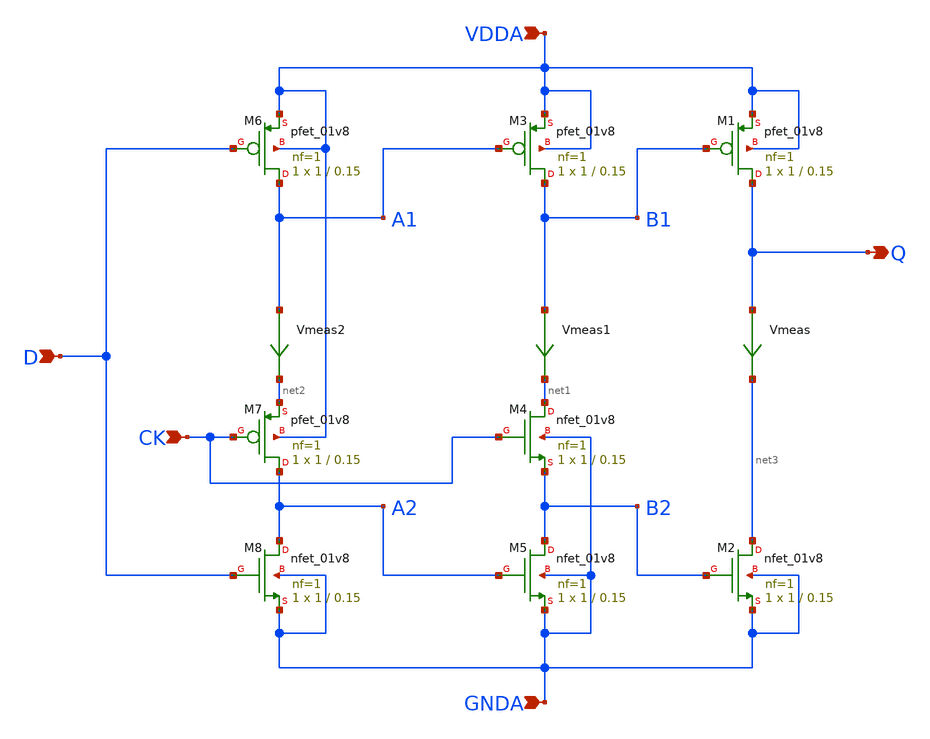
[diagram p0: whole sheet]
** sch_path: projects/pll/divider/xschem_ngspice/TSPC_FF_split_path.sch
**.subckt TSPC_FF_split_path CK D Q VDDA GNDA
*.ipin CK
*.ipin D
*.opin Q
*.ipin VDDA
*.ipin GNDA
XM1 Q B1 VDDA VDDA sky130_fd_pr__pfet_01v8 L=0.15 W=1 nf=1 ad='int((nf+1)/2) * W/nf * 0.29' as='int((nf+2)/2) * W/nf * 0.29'
+ pd='2*int((nf+1)/2) * (W/nf + 0.29)' ps='2*int((nf+2)/2) * (W/nf + 0.29)' nrd='0.29 / W' nrs='0.29 / W'
+ sa=0 sb=0 sd=0 mult=1 m=1
XM4 net1 CK B2 GNDA sky130_fd_pr__nfet_01v8 L=0.15 W=1 nf=1 ad='int((nf+1)/2) * W/nf * 0.29' as='int((nf+2)/2) * W/nf * 0.29'
+ pd='2*int((nf+1)/2) * (W/nf + 0.29)' ps='2*int((nf+2)/2) * (W/nf + 0.29)' nrd='0.29 / W' nrs='0.29 / W'
+ sa=0 sb=0 sd=0 mult=1 m=1
Vmeas Q net3 0
.save i(vmeas)
XM2 net3 B2 GNDA GNDA sky130_fd_pr__nfet_01v8 L=0.15 W=1 nf=1 ad='int((nf+1)/2) * W/nf * 0.29' as='int((nf+2)/2) * W/nf * 0.29'
+ pd='2*int((nf+1)/2) * (W/nf + 0.29)' ps='2*int((nf+2)/2) * (W/nf + 0.29)' nrd='0.29 / W' nrs='0.29 / W'
+ sa=0 sb=0 sd=0 mult=1 m=1
XM3 B1 A1 VDDA VDDA sky130_fd_pr__pfet_01v8 L=0.15 W=1 nf=1 ad='int((nf+1)/2) * W/nf * 0.29' as='int((nf+2)/2) * W/nf * 0.29'
+ pd='2*int((nf+1)/2) * (W/nf + 0.29)' ps='2*int((nf+2)/2) * (W/nf + 0.29)' nrd='0.29 / W' nrs='0.29 / W'
+ sa=0 sb=0 sd=0 mult=1 m=1
XM5 B2 A2 GNDA GNDA sky130_fd_pr__nfet_01v8 L=0.15 W=1 nf=1 ad='int((nf+1)/2) * W/nf * 0.29' as='int((nf+2)/2) * W/nf * 0.29'
+ pd='2*int((nf+1)/2) * (W/nf + 0.29)' ps='2*int((nf+2)/2) * (W/nf + 0.29)' nrd='0.29 / W' nrs='0.29 / W'
+ sa=0 sb=0 sd=0 mult=1 m=1
Vmeas1 B1 net1 0
.save i(vmeas1)
XM6 A1 D VDDA VDDA sky130_fd_pr__pfet_01v8 L=0.15 W=1 nf=1 ad='int((nf+1)/2) * W/nf * 0.29' as='int((nf+2)/2) * W/nf * 0.29'
+ pd='2*int((nf+1)/2) * (W/nf + 0.29)' ps='2*int((nf+2)/2) * (W/nf + 0.29)' nrd='0.29 / W' nrs='0.29 / W'
+ sa=0 sb=0 sd=0 mult=1 m=1
XM8 A2 D GNDA GNDA sky130_fd_pr__nfet_01v8 L=0.15 W=1 nf=1 ad='int((nf+1)/2) * W/nf * 0.29' as='int((nf+2)/2) * W/nf * 0.29'
+ pd='2*int((nf+1)/2) * (W/nf + 0.29)' ps='2*int((nf+2)/2) * (W/nf + 0.29)' nrd='0.29 / W' nrs='0.29 / W'
+ sa=0 sb=0 sd=0 mult=1 m=1
Vmeas2 A1 net2 0
.save i(vmeas2)
XM7 A2 CK net2 VDDA sky130_fd_pr__pfet_01v8 L=0.15 W=1 nf=1 ad='int((nf+1)/2) * W/nf * 0.29' as='int((nf+2)/2) * W/nf * 0.29'
+ pd='2*int((nf+1)/2) * (W/nf + 0.29)' ps='2*int((nf+2)/2) * (W/nf + 0.29)' nrd='0.29 / W' nrs='0.29 / W'
+ sa=0 sb=0 sd=0 mult=1 m=1
**.ends
.end
